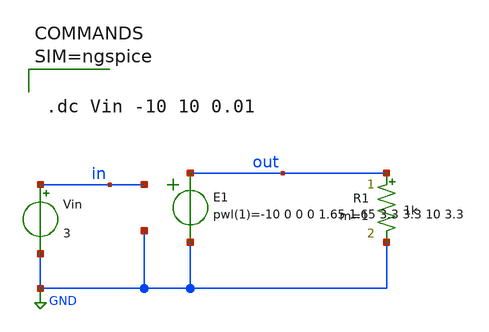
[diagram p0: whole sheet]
** sch_path: designs/libs/untitled-1.sch
**.subckt untitled-1
E1 out GND pwl(1) in GND -10 0 0 0 1.65 1.65 3.3 3.3 10 3.3
R1 out GND 1k m=1
Vin in GND 3
**** begin user architecture code



.dc Vin -10 10 0.01



**** end user architecture code
**.ends
.GLOBAL GND
.end
